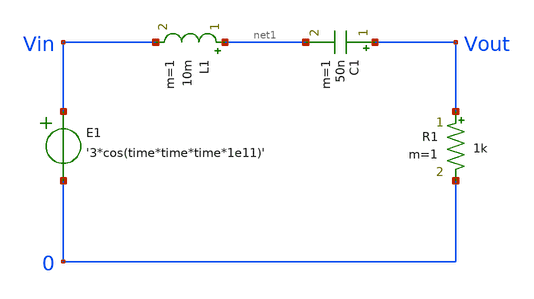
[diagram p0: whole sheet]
** sch_path: lib/Organize_into_Examples_or_pdk_examples/rlc.sch
**.subckt rlc
C1 Vout net1 50n m=1
L1 net1 Vin 10m m=1
R1 Vout 0 1k m=1
E1 Vin 0 VOL=' '3*cos(time*time*time*1e11)' '
**** begin user architecture code


.tran 10n 2000u uic
.save all


**** end user architecture code
**.ends
.end
